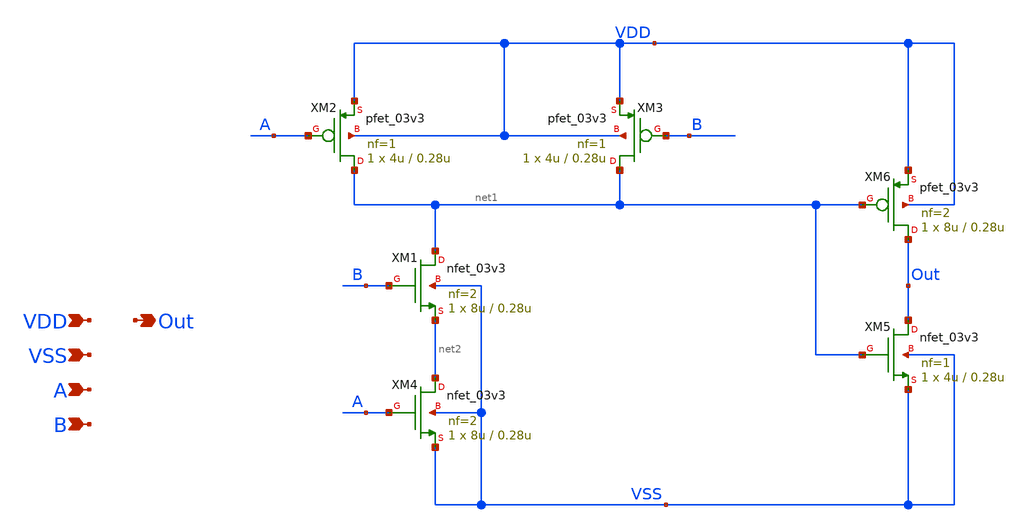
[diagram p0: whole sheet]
** sch_path: designs/digital/schematic/AND_gate.sch
**.subckt AND_gate VDD VSS A B Out
*.ipin VDD
*.ipin VSS
*.ipin A
*.ipin B
*.opin Out
XM1 net1 B net2 VSS nfet_03v3 L=0.28u W=8u nf=2 ad='int((nf+1)/2) * W/nf * 0.18u' as='int((nf+2)/2) * W/nf * 0.18u'
+ pd='2*int((nf+1)/2) * (W/nf + 0.18u)' ps='2*int((nf+2)/2) * (W/nf + 0.18u)' nrd='0.18u / W' nrs='0.18u / W'
+ sa=0 sb=0 sd=0 m=1
XM2 net1 A VDD VDD pfet_03v3 L=0.28u W=4u nf=1 ad='int((nf+1)/2) * W/nf * 0.18u' as='int((nf+2)/2) * W/nf * 0.18u'
+ pd='2*int((nf+1)/2) * (W/nf + 0.18u)' ps='2*int((nf+2)/2) * (W/nf + 0.18u)' nrd='0.18u / W' nrs='0.18u / W'
+ sa=0 sb=0 sd=0 m=1
XM3 net1 B VDD VDD pfet_03v3 L=0.28u W=4u nf=1 ad='int((nf+1)/2) * W/nf * 0.18u' as='int((nf+2)/2) * W/nf * 0.18u'
+ pd='2*int((nf+1)/2) * (W/nf + 0.18u)' ps='2*int((nf+2)/2) * (W/nf + 0.18u)' nrd='0.18u / W' nrs='0.18u / W'
+ sa=0 sb=0 sd=0 m=1
XM4 net2 A VSS VSS nfet_03v3 L=0.28u W=8u nf=2 ad='int((nf+1)/2) * W/nf * 0.18u' as='int((nf+2)/2) * W/nf * 0.18u'
+ pd='2*int((nf+1)/2) * (W/nf + 0.18u)' ps='2*int((nf+2)/2) * (W/nf + 0.18u)' nrd='0.18u / W' nrs='0.18u / W'
+ sa=0 sb=0 sd=0 m=1
XM5 Out net1 VSS VSS nfet_03v3 L=0.28u W=4u nf=1 ad='int((nf+1)/2) * W/nf * 0.18u' as='int((nf+2)/2) * W/nf * 0.18u'
+ pd='2*int((nf+1)/2) * (W/nf + 0.18u)' ps='2*int((nf+2)/2) * (W/nf + 0.18u)' nrd='0.18u / W' nrs='0.18u / W'
+ sa=0 sb=0 sd=0 m=1
XM6 Out net1 VDD VDD pfet_03v3 L=0.28u W=8u nf=2 ad='int((nf+1)/2) * W/nf * 0.18u' as='int((nf+2)/2) * W/nf * 0.18u'
+ pd='2*int((nf+1)/2) * (W/nf + 0.18u)' ps='2*int((nf+2)/2) * (W/nf + 0.18u)' nrd='0.18u / W' nrs='0.18u / W'
+ sa=0 sb=0 sd=0 m=1
**.ends
.end
